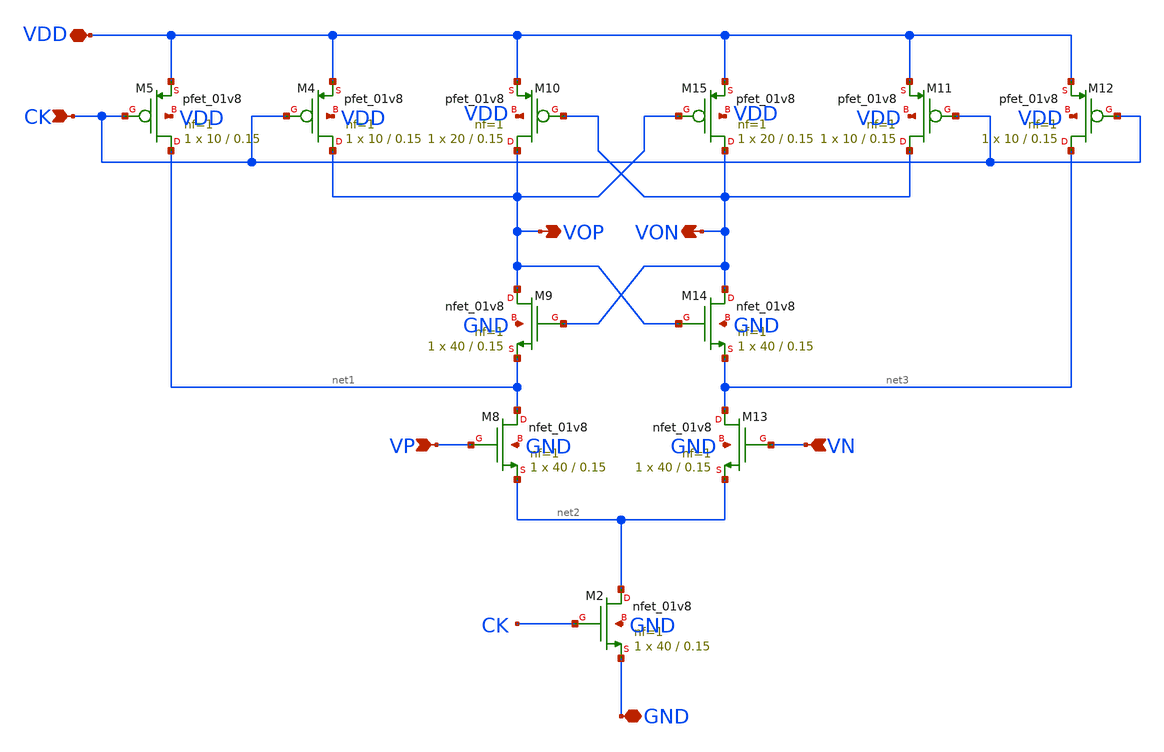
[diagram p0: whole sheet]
** sch_path: xschem/comparator.sch
**.subckt comparator GND VP VOP VON VN VDD CK
*.iopin GND
*.ipin VP
*.opin VOP
*.opin VON
*.ipin VN
*.iopin VDD
*.ipin CK
XM2 net2 CK GND GND sky130_fd_pr__nfet_01v8 L=0.15 W=40 nf=1 ad='int((nf+1)/2) * W/nf * 0.29' as='int((nf+2)/2) * W/nf * 0.29'
+ pd='2*int((nf+1)/2) * (W/nf + 0.29)' ps='2*int((nf+2)/2) * (W/nf + 0.29)' nrd='0.29 / W' nrs='0.29 / W'
+ sa=0 sb=0 sd=0 mult=1 m=1
XM4 VOP CK VDD VDD sky130_fd_pr__pfet_01v8 L=0.15 W=10 nf=1 ad='int((nf+1)/2) * W/nf * 0.29' as='int((nf+2)/2) * W/nf * 0.29'
+ pd='2*int((nf+1)/2) * (W/nf + 0.29)' ps='2*int((nf+2)/2) * (W/nf + 0.29)' nrd='0.29 / W' nrs='0.29 / W'
+ sa=0 sb=0 sd=0 mult=1 m=1
XM5 net1 CK VDD VDD sky130_fd_pr__pfet_01v8 L=0.15 W=10 nf=1 ad='int((nf+1)/2) * W/nf * 0.29' as='int((nf+2)/2) * W/nf * 0.29'
+ pd='2*int((nf+1)/2) * (W/nf + 0.29)' ps='2*int((nf+2)/2) * (W/nf + 0.29)' nrd='0.29 / W' nrs='0.29 / W'
+ sa=0 sb=0 sd=0 mult=1 m=1
XM8 net1 VP net2 GND sky130_fd_pr__nfet_01v8 L=0.15 W=40 nf=1 ad='int((nf+1)/2) * W/nf * 0.29' as='int((nf+2)/2) * W/nf * 0.29'
+ pd='2*int((nf+1)/2) * (W/nf + 0.29)' ps='2*int((nf+2)/2) * (W/nf + 0.29)' nrd='0.29 / W' nrs='0.29 / W'
+ sa=0 sb=0 sd=0 mult=1 m=1
XM9 VOP VON net1 GND sky130_fd_pr__nfet_01v8 L=0.15 W=40 nf=1 ad='int((nf+1)/2) * W/nf * 0.29' as='int((nf+2)/2) * W/nf * 0.29'
+ pd='2*int((nf+1)/2) * (W/nf + 0.29)' ps='2*int((nf+2)/2) * (W/nf + 0.29)' nrd='0.29 / W' nrs='0.29 / W'
+ sa=0 sb=0 sd=0 mult=1 m=1
XM10 VOP VON VDD VDD sky130_fd_pr__pfet_01v8 L=0.15 W=20 nf=1 ad='int((nf+1)/2) * W/nf * 0.29' as='int((nf+2)/2) * W/nf * 0.29'
+ pd='2*int((nf+1)/2) * (W/nf + 0.29)' ps='2*int((nf+2)/2) * (W/nf + 0.29)' nrd='0.29 / W' nrs='0.29 / W'
+ sa=0 sb=0 sd=0 mult=1 m=1
XM11 VON CK VDD VDD sky130_fd_pr__pfet_01v8 L=0.15 W=10 nf=1 ad='int((nf+1)/2) * W/nf * 0.29' as='int((nf+2)/2) * W/nf * 0.29'
+ pd='2*int((nf+1)/2) * (W/nf + 0.29)' ps='2*int((nf+2)/2) * (W/nf + 0.29)' nrd='0.29 / W' nrs='0.29 / W'
+ sa=0 sb=0 sd=0 mult=1 m=1
XM12 net3 CK VDD VDD sky130_fd_pr__pfet_01v8 L=0.15 W=10 nf=1 ad='int((nf+1)/2) * W/nf * 0.29' as='int((nf+2)/2) * W/nf * 0.29'
+ pd='2*int((nf+1)/2) * (W/nf + 0.29)' ps='2*int((nf+2)/2) * (W/nf + 0.29)' nrd='0.29 / W' nrs='0.29 / W'
+ sa=0 sb=0 sd=0 mult=1 m=1
XM13 net3 VN net2 GND sky130_fd_pr__nfet_01v8 L=0.15 W=40 nf=1 ad='int((nf+1)/2) * W/nf * 0.29' as='int((nf+2)/2) * W/nf * 0.29'
+ pd='2*int((nf+1)/2) * (W/nf + 0.29)' ps='2*int((nf+2)/2) * (W/nf + 0.29)' nrd='0.29 / W' nrs='0.29 / W'
+ sa=0 sb=0 sd=0 mult=1 m=1
XM14 VON VOP net3 GND sky130_fd_pr__nfet_01v8 L=0.15 W=40 nf=1 ad='int((nf+1)/2) * W/nf * 0.29' as='int((nf+2)/2) * W/nf * 0.29'
+ pd='2*int((nf+1)/2) * (W/nf + 0.29)' ps='2*int((nf+2)/2) * (W/nf + 0.29)' nrd='0.29 / W' nrs='0.29 / W'
+ sa=0 sb=0 sd=0 mult=1 m=1
XM15 VON VOP VDD VDD sky130_fd_pr__pfet_01v8 L=0.15 W=20 nf=1 ad='int((nf+1)/2) * W/nf * 0.29' as='int((nf+2)/2) * W/nf * 0.29'
+ pd='2*int((nf+1)/2) * (W/nf + 0.29)' ps='2*int((nf+2)/2) * (W/nf + 0.29)' nrd='0.29 / W' nrs='0.29 / W'
+ sa=0 sb=0 sd=0 mult=1 m=1
**.ends
.end
